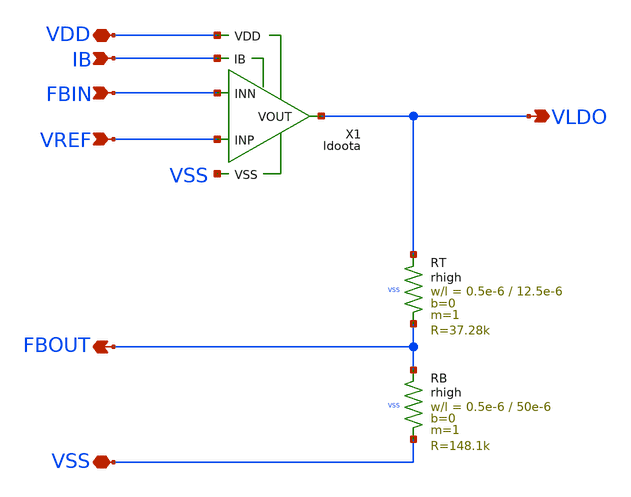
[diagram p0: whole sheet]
** sch_path: ip/ldo/xschem/ldo.sch
**.subckt ldo VSS VDD VLDO VREF FBOUT FBIN IB
*.iopin VSS
*.iopin VDD
*.opin VLDO
*.ipin VREF
*.opin FBOUT
*.ipin FBIN
*.ipin IB
X1 VDD VSS VLDO IB FBIN VREF ldoota
XRT VLDO FBOUT VSS rhigh w=0.5e-6 l=12.5e-6 m=1 b=0 mm_ok=1
XRB FBOUT VSS VSS rhigh w=0.5e-6 l=50e-6 m=1 b=0 mm_ok=1
**.ends

* expanding   symbol:  ldoota.sym # of pins=6
** sym_path: ip/ldo/xschem/ldoota.sym
** sch_path: ip/ldo/xschem/ldoota.sch
.subckt ldoota VDD VSS VOUT IB INN INP
*.ipin IB
*.iopin VDD
*.iopin VSS
*.iopin INP
*.iopin INN
*.iopin VOUT
XMMIRL1 net4 net1 VDD VDD sg13_hv_pmos w=10u l=2u ng=1 m=2 mm_ok=1
XMMIRR net2 net2 VDD VDD sg13_hv_pmos w=10u l=2u ng=1 m=2 mm_ok=1
XMMIRL net1 net1 VDD VDD sg13_hv_pmos w=10u l=2u ng=1 m=2 mm_ok=1
XMO vot net2 VDD VDD sg13_hv_pmos w=10u l=2u ng=1 m=10 mm_ok=1
XMOT VOUT vot VDD VDD sg13_hv_pmos w=10u l=0.5u ng=1 m=40 mm_ok=1
XMDL net1 INP net3 VSS sg13_hv_nmos w=10u l=2u ng=1 m=10 mm_ok=1
XMDR net2 INN net3 VSS sg13_hv_nmos w=10u l=2u ng=1 m=10 mm_ok=1
XMMIR2 net3 IB VSS VSS sg13_hv_nmos w=10u l=2u ng=1 m=2 mm_ok=1
XMOB VOUT IB VSS VSS sg13_hv_nmos w=10u l=2u ng=1 m=8 mm_ok=1
XMMIR3 vot net4 VSS VSS sg13_hv_nmos w=10u l=2u ng=1 m=10 mm_ok=1
XMMIRL2 net4 net4 VSS VSS sg13_hv_nmos w=10u l=2u ng=1 m=2 mm_ok=1
XMMIR1 IB IB VSS VSS sg13_hv_nmos w=10u l=2u ng=1 m=2 mm_ok=1
XR1 VOUT net5 VSS rppd w=1e-6 l=10.6e-6 m=1 b=0 mm_ok=1
XC1 net5 vot cap_cmim w=24e-6 l=24e-6 m=9 mm_ok=1
.ends

.end
